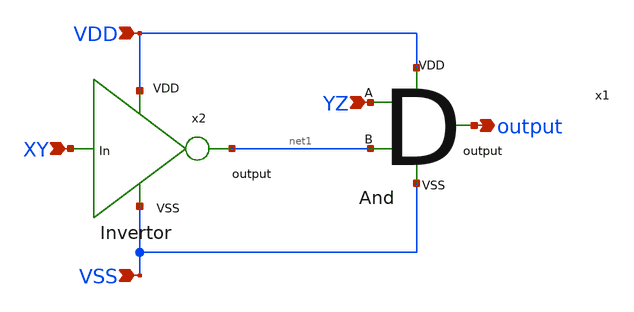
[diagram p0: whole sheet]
** sch_path: activities/opamp3AKAM/yGates.sch
**.subckt yGates VDD VSS YZ XY output
*.ipin VDD
*.ipin VSS
*.ipin YZ
*.ipin XY
*.opin output
x1 YZ VDD net1 output VSS andGate
x2 VDD net1 XY VSS invertor
**.ends
.end
